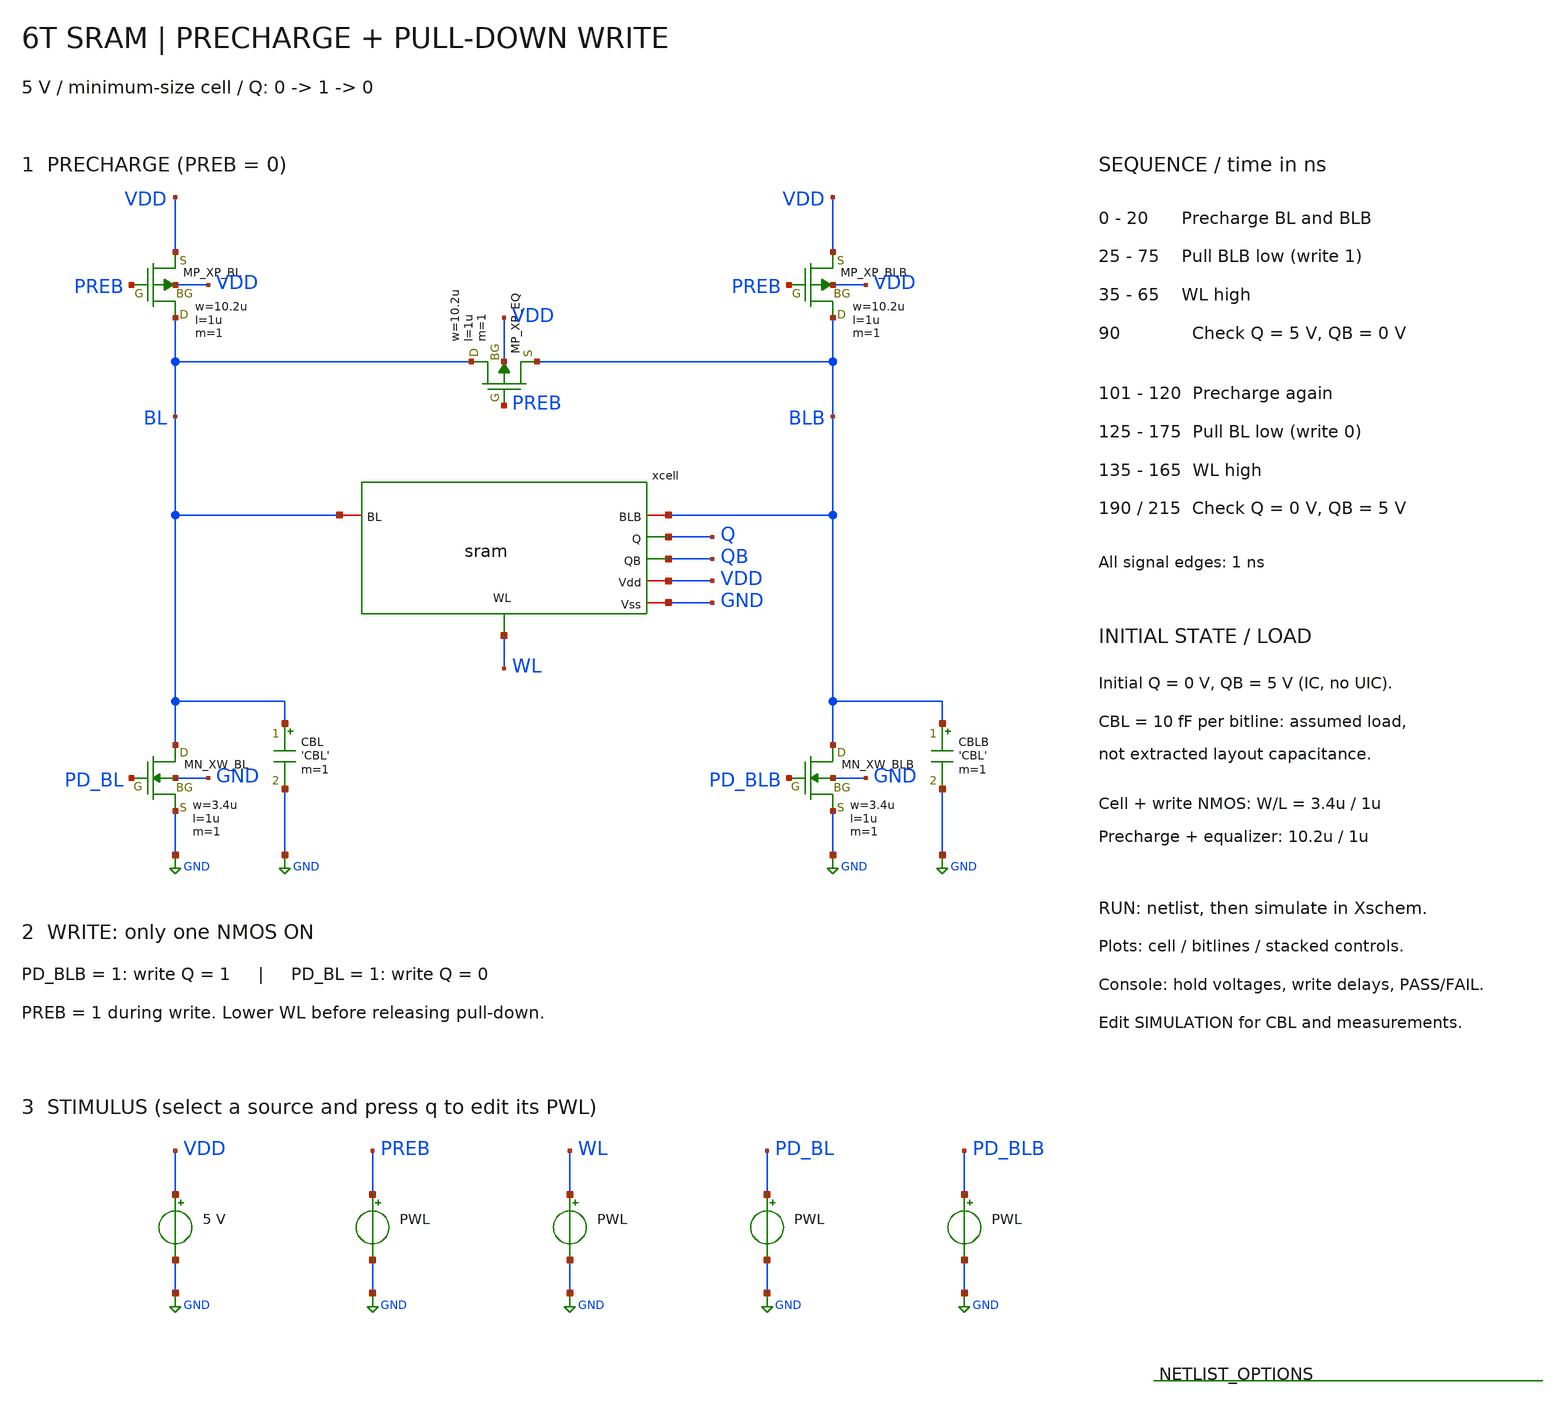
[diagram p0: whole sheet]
** sch_path: member_project/SRAM/PenguinEino/learning/schematics/sram_tb_tran_write_pulldown.sch
**.subckt sram_tb_tran_write_pulldown
XXP_BL BL PREB VDD VDD PMOS w=10.2u l=1u nrd=0 nrs=0 m=1
XXW_BL BL PD_BL GND GND NMOS w=3.4u l=1u nrd=0 nrs=0 m=1
XXP_BLB BLB PREB VDD VDD PMOS w=10.2u l=1u nrd=0 nrs=0 m=1
XXW_BLB BLB PD_BLB GND GND NMOS w=3.4u l=1u nrd=0 nrs=0 m=1
XXP_EQ BL PREB BLB VDD PMOS w=10.2u l=1u nrd=0 nrs=0 m=1
xcell WL VDD BLB Q QB BL GND sram
CBL BL GND 'CBL' m=1
CBLB BLB GND 'CBL' m=1
VVDD VDD GND 5
VPREB PREB GND PWL(0 0 20n 0 21n 5 100n 5 101n 0 120n 0 121n 5 220n 5)
VWL WL GND PWL(0 0 35n 0 36n 5 65n 5 66n 0 135n 0 136n 5 165n 5 166n 0 220n 0)
VPD_BL PD_BL GND PWL(0 0 125n 0 126n 5 175n 5 176n 0 220n 0)
VPD_BLB PD_BLB GND PWL(0 0 25n 0 26n 5 75n 5 76n 0 220n 0)
**** begin user architecture code
 .include $::LIB/ip62_models

.param CBL=10f
.ic v(Q)=0 v(QB)=5
.control
save all
tran 0.05n 220n
meas tran q_initial find v(Q) at=19n
meas tran qb_initial find v(QB) at=19n
meas tran q_hold_1 find v(Q) at=90n
meas tran qb_hold_1 find v(QB) at=90n
meas tran q_hold_0 find v(Q) at=190n
meas tran qb_hold_0 find v(QB) at=190n
meas tran q_final find v(Q) at=215n
meas tran qb_final find v(QB) at=215n
meas tran t_write_1 trig v(WL) val=2.5 rise=1 targ v(Q) val=2.5 rise=1
meas tran t_write_0 trig v(WL) val=2.5 rise=2 targ v(Q) val=2.5 fall=1 td=120n
if q_initial < 0.5 and qb_initial > 4.5 and q_hold_1 > 4.5 and qb_hold_1 < 0.5 and q_hold_0 < 0.5
+ and qb_hold_0 > 4.5 and q_final < 0.5 and qb_final > 4.5
  echo PASS: initial state, write 1, write 0 and hold checks
else
  echo FAIL: inspect Q/QB and bitline plots
end
let PREB_trace = v(PREB)/5+6
let WL_trace = v(WL)/5+4
let PD_BL_trace = v(PD_BL)/5+2
let PD_BLB_trace = v(PD_BLB)/5
write sram_tb_tran_write_pulldown.raw
plot v(Q) v(QB) ylimit -0.5 5.5 title 'CELL: Q 0 -> 1 -> 0; hold checks at 90/190/215 ns'
plot v(BL) v(BLB) ylimit -0.5 5.5 title 'BITLINES: precharged, then only one side pulled low'
plot PREB_trace WL_trace PD_BL_trace PD_BLB_trace ylimit -0.3 7.3 title 'CONTROLS: PREB +6 / WL +4 / PD_BL +2 / PD_BLB +0 (normalized)'
.endc

**** end user architecture code
**.ends
.GLOBAL GND
.end
